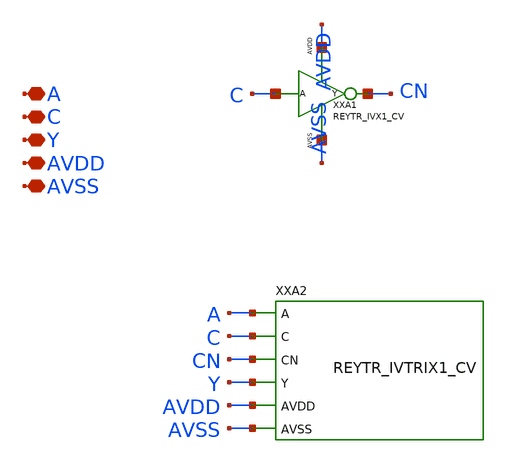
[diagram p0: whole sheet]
** sch_path: design/REY_TR_SKY130A/REYTR_IVTRICX1_CV.sch
**.subckt REYTR_IVTRICX1_CV A C Y AVDD AVSS
*.iopin A
*.iopin C
*.iopin Y
*.iopin AVDD
*.iopin AVSS
XXA1 C CN AVDD AVSS REYTR_IVX1_CV
XXA2 A C CN Y AVDD AVSS REYTR_IVTRIX1_CV xoffset=0 yoffset=0 angle=0
**.ends
.end
